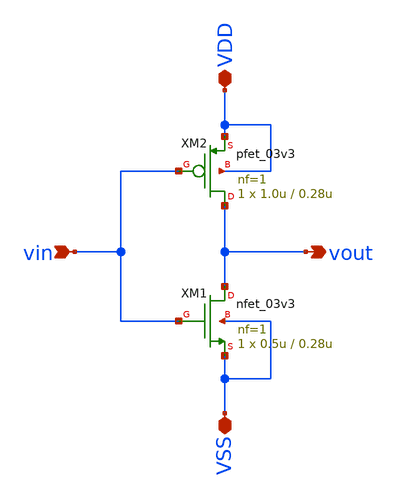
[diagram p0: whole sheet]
** sch_path: designs/libs/core_analog/inv_x1/inv_x1.sch
**.subckt inv_x1 VDD VSS vin vout
*.iopin VDD
*.iopin VSS
*.ipin vin
*.opin vout
XM1 vout vin VSS VSS nfet_03v3 L=0.28u W=0.5u nf=1 ad='int((nf+1)/2) * W/nf * 0.18u' as='int((nf+2)/2) * W/nf * 0.18u'
+ pd='2*int((nf+1)/2) * (W/nf + 0.18u)' ps='2*int((nf+2)/2) * (W/nf + 0.18u)' nrd='0.18u / W' nrs='0.18u / W'
+ sa=0 sb=0 sd=0 m=1
XM2 vout vin VDD VDD pfet_03v3 L=0.28u W=1.0u nf=1 ad='int((nf+1)/2) * W/nf * 0.18u' as='int((nf+2)/2) * W/nf * 0.18u'
+ pd='2*int((nf+1)/2) * (W/nf + 0.18u)' ps='2*int((nf+2)/2) * (W/nf + 0.18u)' nrd='0.18u / W' nrs='0.18u / W'
+ sa=0 sb=0 sd=0 m=1
**.ends
.end
